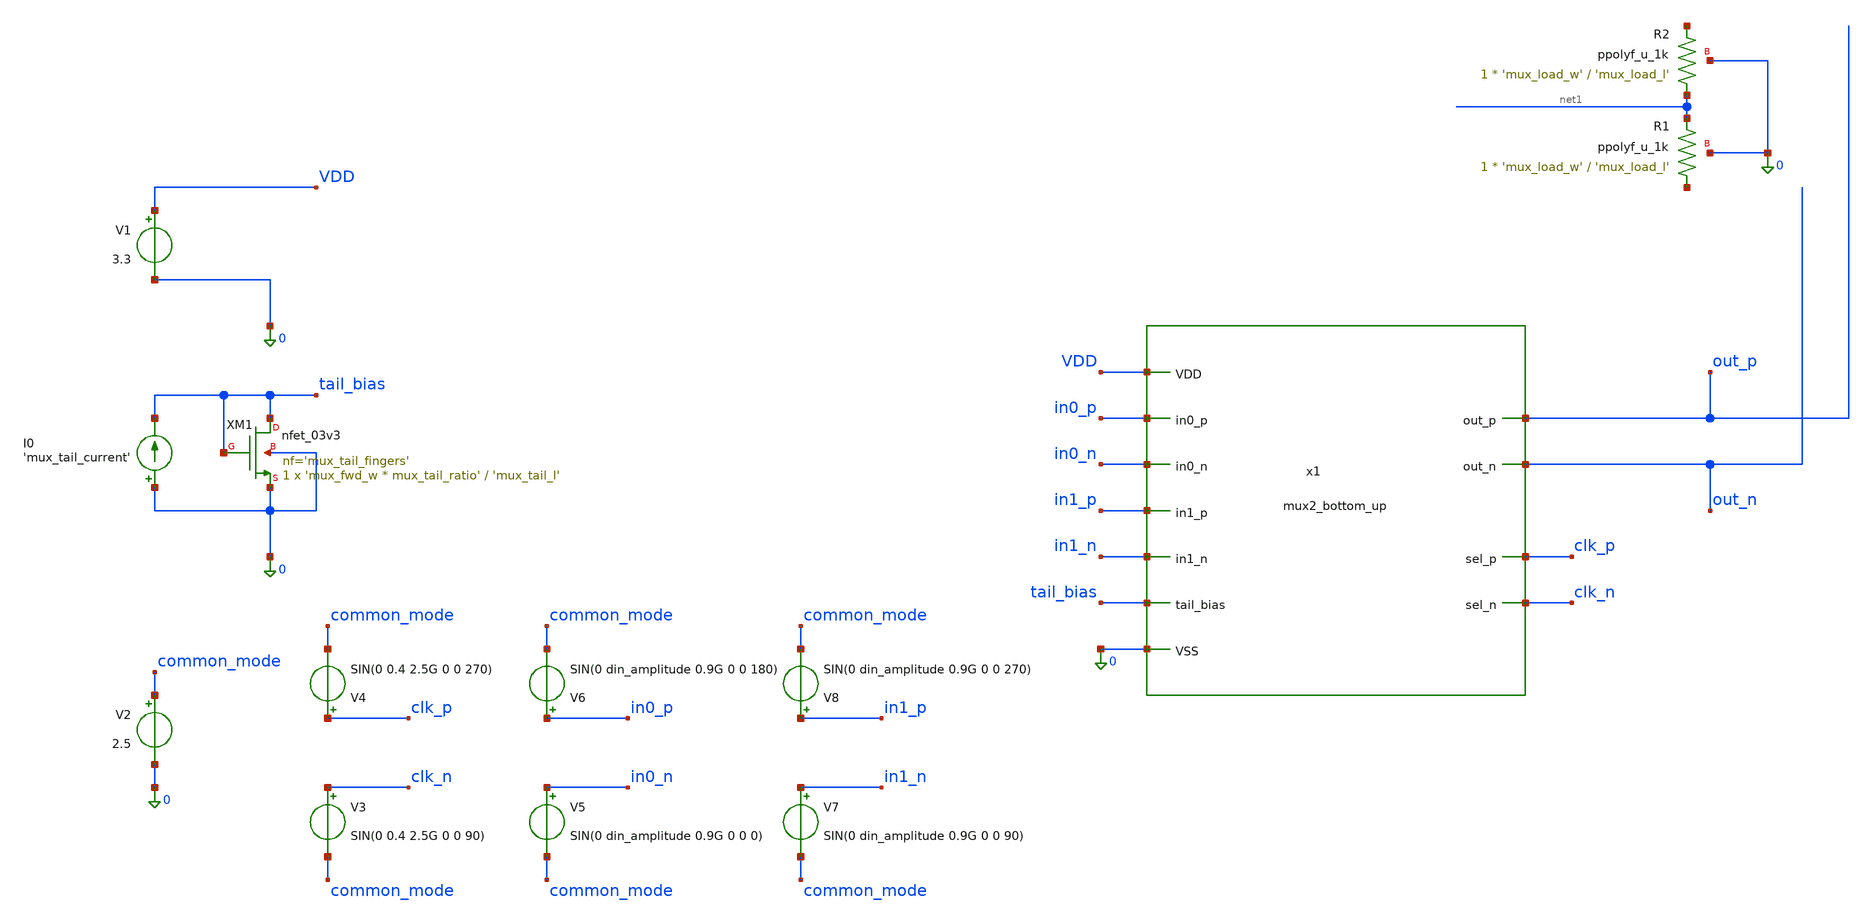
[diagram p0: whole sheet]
** sch_path: xschem/mux2_bottom_tb.sch
**.subckt mux2_bottom_tb
x1 VDD clk_p clk_n out_n out_p in0_n in1_p in0_p in1_n tail_bias 0 mux2_bottom_up
XM1 tail_bias tail_bias 0 0 nfet_03v3 L='mux_tail_l' W='mux_fwd_w * mux_tail_ratio' nf='mux_tail_fingers'
+ ad='int((nf+1)/2) * W/nf * 0.18u' as='int((nf+2)/2) * W/nf * 0.18u' pd='2*int((nf+1)/2) * (W/nf + 0.18u)'
+ ps='2*int((nf+2)/2) * (W/nf + 0.18u)' nrd='0.18u / W' nrs='0.18u / W' sa=0 sb=0 sd=0 m=1
V1 VDD 0 3.3
I0 0 tail_bias 'mux_tail_current'
V3 clk_n common_mode SIN(0 0.4 2.5G 0 0 90)
V4 clk_p common_mode SIN(0 0.4 2.5G 0 0 270)
V2 common_mode 0 2.5
XR1 net2 net1 0 ppolyf_u_1k r_width='mux_load_w' r_length='mux_load_l' m=1
XR2 net1 net3 0 ppolyf_u_1k r_width='mux_load_w' r_length='mux_load_l' m=1
V5 in0_n common_mode SIN(0 din_amplitude 0.9G 0 0 0)
V6 in0_p common_mode SIN(0 din_amplitude 0.9G 0 0 180)
V7 in1_n common_mode SIN(0 din_amplitude 0.9G 0 0 90)
V8 in1_p common_mode SIN(0 din_amplitude 0.9G 0 0 270)
**** begin user architecture code
 .include $::180MCU_MODELS/design.ngspice
.lib $::180MCU_MODELS/sm141064.ngspice typical
.lib $::180MCU_MODELS/sm141064.ngspice res_typical


.option savecurrents

.param mux_fwd_w=4u
.param mux_pf_ratio='1'
.param mux_fwd_fingers=1
.param mux_pf_fingers=1
.param mux_tail_fingers=20
.param mux_sel_ratio=1
.param mux_sel_fingers=1
.param mux_tail_ratio=50
.param mux_tail_l=1u
.param mux_load_w=1u
.param mux_load_r=12k
.param mux_load_l='mux_load_r/1000 * mux_load_w'
.param din_amplitude=0.4
.param mux_tail_current=128u

.nodeset v(net1)=2.5

.control
save all
tran 5p 50n
*plot clk_p clk_n out_p out_n in0_p in0_n in1_p in1_n v(out_p, out_n)
plot clk_p out_p out_n in0_p in1_p v(out_p, out_n)
plot clk_p in0_p in1_p v(out_p, out_n) x1.net3 x1.net5
write mux2_bottom_tb.raw
.endc
**** end user architecture code
**.ends

* expanding   symbol:  mux2_bottom_up.sym # of pins=11
** sym_path: xschem/mux2_bottom_up.sym
** sch_path: xschem/mux2_bottom_up.sch
.subckt mux2_bottom_up VDD sel_p sel_n out_n out_p in0_n in1_p in0_p in1_n tail_bias VSS
*.ipin VSS
*.ipin VDD
*.opin out_n
*.opin out_p
*.ipin in0_p
*.ipin in0_n
*.ipin sel_p
*.ipin sel_n
*.ipin tail_bias
*.ipin in1_p
*.ipin in1_n
XM1 net2 in0_p net1 VSS nfet_03v3 L=0.28u W='mux_fwd_w' nf='mux_fwd_fingers' ad='int((nf+1)/2) * W/nf * 0.18u'
+ as='int((nf+2)/2) * W/nf * 0.18u' pd='2*int((nf+1)/2) * (W/nf + 0.18u)' ps='2*int((nf+2)/2) * (W/nf + 0.18u)'
+ nrd='0.18u / W' nrs='0.18u / W' sa=0 sb=0 sd=0 m=1
XM5 net1 tail_bias VSS VSS nfet_03v3 L='mux_tail_l' W='mux_fwd_w * mux_tail_ratio' nf='mux_tail_fingers'
+ ad='int((nf+1)/2) * W/nf * 0.18u' as='int((nf+2)/2) * W/nf * 0.18u' pd='2*int((nf+1)/2) * (W/nf + 0.18u)'
+ ps='2*int((nf+2)/2) * (W/nf + 0.18u)' nrd='0.18u / W' nrs='0.18u / W' sa=0 sb=0 sd=0 m=1
XM2 net5 in0_n net1 VSS nfet_03v3 L=0.28u W='mux_fwd_w' nf='mux_fwd_fingers' ad='int((nf+1)/2) * W/nf * 0.18u'
+ as='int((nf+2)/2) * W/nf * 0.18u' pd='2*int((nf+1)/2) * (W/nf + 0.18u)' ps='2*int((nf+2)/2) * (W/nf + 0.18u)'
+ nrd='0.18u / W' nrs='0.18u / W' sa=0 sb=0 sd=0 m=1
XR1 out_n VDD VSS ppolyf_u_1k r_width='mux_load_w' r_length='mux_load_l' m=1
XR2 out_p VDD VSS ppolyf_u_1k r_width='mux_load_w' r_length='mux_load_l' m=1
XM6 out_n sel_n net2 VSS nfet_03v3 L=0.28u W='mux_fwd_w * mux_sel_ratio' nf='mux_sel_fingers' ad='int((nf+1)/2) * W/nf * 0.18u'
+ as='int((nf+2)/2) * W/nf * 0.18u' pd='2*int((nf+1)/2) * (W/nf + 0.18u)' ps='2*int((nf+2)/2) * (W/nf + 0.18u)'
+ nrd='0.18u / W' nrs='0.18u / W' sa=0 sb=0 sd=0 m=1
XM7 out_p sel_n net5 VSS nfet_03v3 L=0.28u W='mux_fwd_w * mux_sel_ratio' nf='mux_sel_fingers' ad='int((nf+1)/2) * W/nf * 0.18u'
+ as='int((nf+2)/2) * W/nf * 0.18u' pd='2*int((nf+1)/2) * (W/nf + 0.18u)' ps='2*int((nf+2)/2) * (W/nf + 0.18u)'
+ nrd='0.18u / W' nrs='0.18u / W' sa=0 sb=0 sd=0 m=1
XM3 net3 in1_p net1 VSS nfet_03v3 L=0.28u W='mux_fwd_w' nf='mux_fwd_fingers' ad='int((nf+1)/2) * W/nf * 0.18u'
+ as='int((nf+2)/2) * W/nf * 0.18u' pd='2*int((nf+1)/2) * (W/nf + 0.18u)' ps='2*int((nf+2)/2) * (W/nf + 0.18u)'
+ nrd='0.18u / W' nrs='0.18u / W' sa=0 sb=0 sd=0 m=1
XM4 net4 in1_n net1 VSS nfet_03v3 L=0.28u W='mux_fwd_w' nf='mux_fwd_fingers' ad='int((nf+1)/2) * W/nf * 0.18u'
+ as='int((nf+2)/2) * W/nf * 0.18u' pd='2*int((nf+1)/2) * (W/nf + 0.18u)' ps='2*int((nf+2)/2) * (W/nf + 0.18u)'
+ nrd='0.18u / W' nrs='0.18u / W' sa=0 sb=0 sd=0 m=1
XM8 out_n sel_p net3 VSS nfet_03v3 L=0.28u W='mux_fwd_w * mux_sel_ratio' nf='mux_sel_fingers' ad='int((nf+1)/2) * W/nf * 0.18u'
+ as='int((nf+2)/2) * W/nf * 0.18u' pd='2*int((nf+1)/2) * (W/nf + 0.18u)' ps='2*int((nf+2)/2) * (W/nf + 0.18u)'
+ nrd='0.18u / W' nrs='0.18u / W' sa=0 sb=0 sd=0 m=1
XM9 out_p sel_p net4 VSS nfet_03v3 L=0.28u W='mux_fwd_w * mux_sel_ratio' nf='mux_sel_fingers' ad='int((nf+1)/2) * W/nf * 0.18u'
+ as='int((nf+2)/2) * W/nf * 0.18u' pd='2*int((nf+1)/2) * (W/nf + 0.18u)' ps='2*int((nf+2)/2) * (W/nf + 0.18u)'
+ nrd='0.18u / W' nrs='0.18u / W' sa=0 sb=0 sd=0 m=1
.ends

.end
